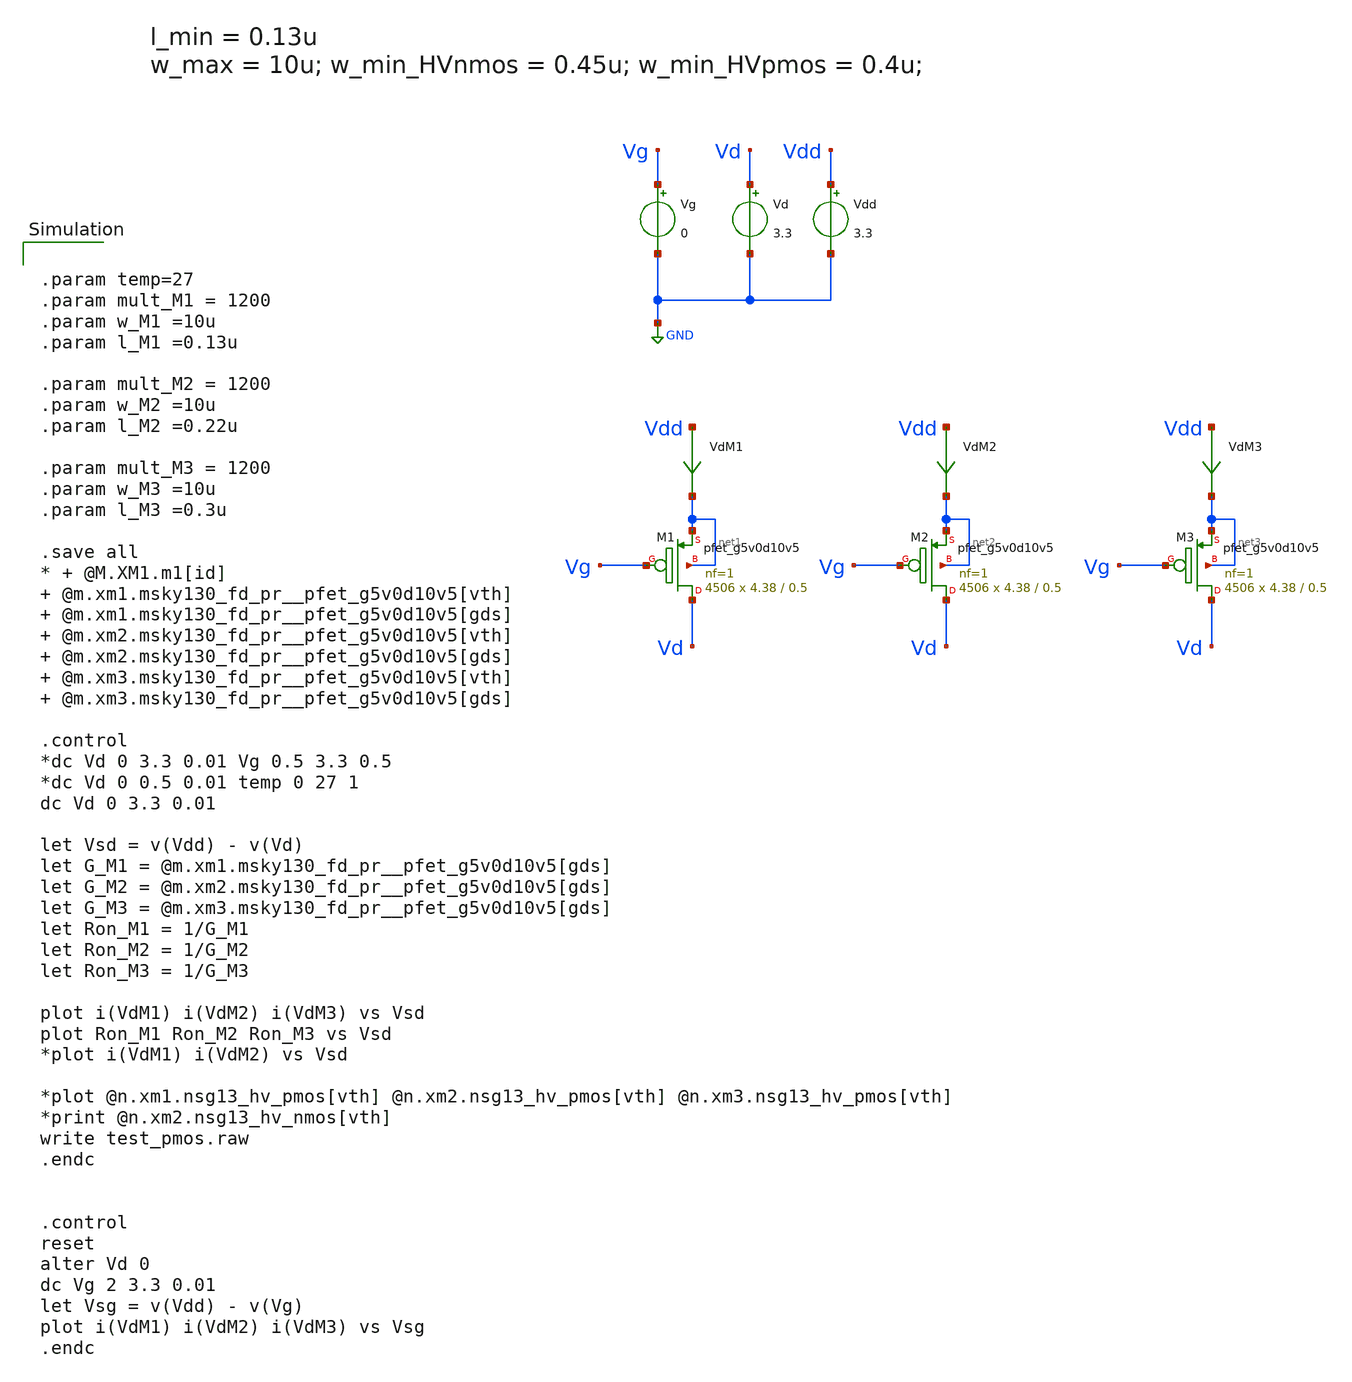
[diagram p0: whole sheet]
** sch_path: xschem/TB_hvPMOS_charact_SKY130.sch
.lib $::SKYWATER_MODELS/sky130.lib.spice tt
.include $::SKYWATER_STDCELLS/sky130_fd_sc_hd.spice

**.subckt TB_hvPMOS_charact_SKY130
Vg Vg GND 0
Vd Vd GND 3.3
Vdd Vdd GND 3.3
VdM1 Vdd net1 0
.save i(vdm1)
VdM2 Vdd net2 0
.save i(vdm2)
VdM3 Vdd net3 0
.save i(vdm3)
XM1 Vd Vg net1 net1 sky130_fd_pr__pfet_g5v0d10v5 L=0.5 W=4.38 nf=1 ad='int((nf+1)/2) * W/nf * 0.29' as='int((nf+2)/2) * W/nf * 0.29'
+ pd='2*int((nf+1)/2) * (W/nf + 0.29)' ps='2*int((nf+2)/2) * (W/nf + 0.29)' nrd='0.29 / W' nrs='0.29 / W'
+ sa=0 sb=0 sd=0 mult=4506 m=4506
XM2 Vd Vg net2 net2 sky130_fd_pr__pfet_g5v0d10v5 L=0.5 W=4.38 nf=1 ad='int((nf+1)/2) * W/nf * 0.29' as='int((nf+2)/2) * W/nf * 0.29'
+ pd='2*int((nf+1)/2) * (W/nf + 0.29)' ps='2*int((nf+2)/2) * (W/nf + 0.29)' nrd='0.29 / W' nrs='0.29 / W'
+ sa=0 sb=0 sd=0 mult=4506 m=4506
XM3 Vd Vg net3 net3 sky130_fd_pr__pfet_g5v0d10v5 L=0.5 W=4.38 nf=1 ad='int((nf+1)/2) * W/nf * 0.29' as='int((nf+2)/2) * W/nf * 0.29'
+ pd='2*int((nf+1)/2) * (W/nf + 0.29)' ps='2*int((nf+2)/2) * (W/nf + 0.29)' nrd='0.29 / W' nrs='0.29 / W'
+ sa=0 sb=0 sd=0 mult=4506 m=4506
**** begin user architecture code


.param temp=27
.param mult_M1 = 1200
.param w_M1 =10u
.param l_M1 =0.13u

.param mult_M2 = 1200
.param w_M2 =10u
.param l_M2 =0.22u

.param mult_M3 = 1200
.param w_M3 =10u
.param l_M3 =0.3u

.save all
* + @M.XM1.m1[id]  @m.xm1.msky130_fd_pr__pfet_g5v0d10v5[vth]
*+  @m.xm1.msky130_fd_pr__pfet_g5v0d10v5[gds]  @m.xm2.msky130_fd_pr__pfet_g5v0d10v5[vth]  @m.xm2.msky130_fd_pr__pfet_g5v0d10v5[gds]
*+  @m.xm3.msky130_fd_pr__pfet_g5v0d10v5[vth]  @m.xm3.msky130_fd_pr__pfet_g5v0d10v5[gds]

.control
*dc Vd 0 3.3 0.01 Vg 0.5 3.3 0.5
*dc Vd 0 0.5 0.01 temp 0 27 1
dc Vd 0 3.3 0.01

let Vsd = v(Vdd) - v(Vd)
let G_M1 = @m.xm1.msky130_fd_pr__pfet_g5v0d10v5[gds]
let G_M2 = @m.xm2.msky130_fd_pr__pfet_g5v0d10v5[gds]
let G_M3 = @m.xm3.msky130_fd_pr__pfet_g5v0d10v5[gds]
let Ron_M1 = 1/G_M1
let Ron_M2 = 1/G_M2
let Ron_M3 = 1/G_M3

plot i(VdM1) i(VdM2) i(VdM3) vs Vsd
plot Ron_M1 Ron_M2 Ron_M3 vs Vsd
*plot i(VdM1) i(VdM2) vs Vsd

*plot @n.xm1.nsg13_hv_pmos[vth] @n.xm2.nsg13_hv_pmos[vth] @n.xm3.nsg13_hv_pmos[vth]
*print @n.xm2.nsg13_hv_nmos[vth]
write test_pmos.raw
.endc


.control
reset
alter Vd 0
dc Vg 2 3.3 0.01
let Vsg = v(Vdd) - v(Vg)
plot i(VdM1) i(VdM2) i(VdM3) vs Vsg
.endc



**** end user architecture code
**.ends
.GLOBAL GND
.end
